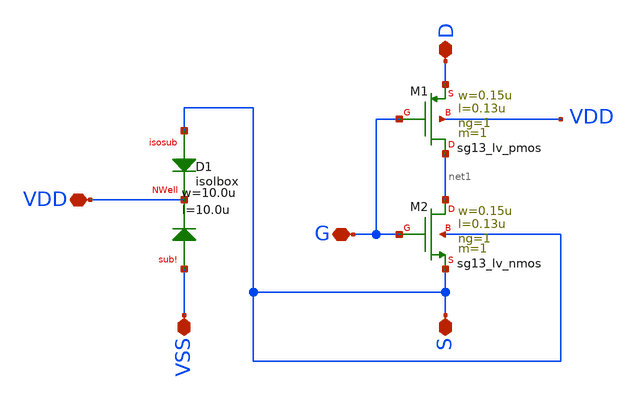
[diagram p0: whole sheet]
** sch_path: ihp-sg13g2/schematic/xschem/sg13_dnwell_inv.sch
**.subckt sg13_dnwell_inv VSS S VDD G D
*.iopin VSS
*.iopin S
*.iopin VDD
*.iopin G
*.iopin D
XD1 S VDD VSS isolbox l=10.0u w=10.0u
XM1 net1 G D VDD sg13_lv_pmos w=0.15u l=0.13u ng=1 m=1 mm_ok=1
XM2 net1 G S S sg13_lv_nmos w=0.15u l=0.13u ng=1 m=1 mm_ok=1
**.ends
.end
